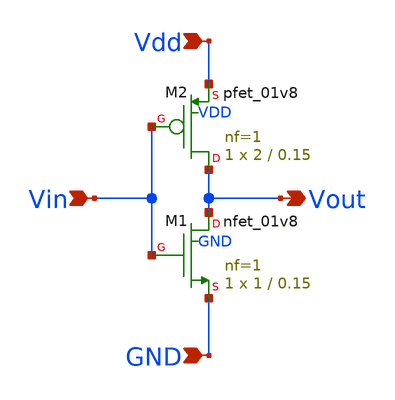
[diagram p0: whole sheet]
** sch_path: 1/xschem/nand.sch
**.subckt nand Vout Vdd GND Vin
*.opin Vout
*.ipin Vdd
*.ipin GND
*.ipin Vin
XM1 Vout Vin GND GND sky130_fd_pr__nfet_01v8 L=0.15 W=1 nf=1 ad='int((1 + 1)/2) * 1 / 1 * 0.29' as='int((1 + 2)/2) * 1 / 1 * 0.29'
+ pd='2*int((1 + 1)/2) * (1 / 1 + 0.29)' ps='2*int((1 + 2)/2) * (1 / 1 + 0.29)' nrd='0.29 / 1 ' nrs='0.29 / 1 '
+ sa=0 sb=0 sd=0 mult=1 m=1
XM2 Vout Vin Vdd VDD sky130_fd_pr__pfet_01v8 L=0.15 W=2 nf=1 ad='int((1 + 1)/2) * 2 / 1 * 0.29' as='int((1 + 2)/2) * 2 / 1 * 0.29'
+ pd='2*int((1 + 1)/2) * (2 / 1 + 0.29)' ps='2*int((1 + 2)/2) * (2 / 1 + 0.29)' nrd='0.29 / 2 ' nrs='0.29 / 2 '
+ sa=0 sb=0 sd=0 mult=1 m=1
**.ends
.end
